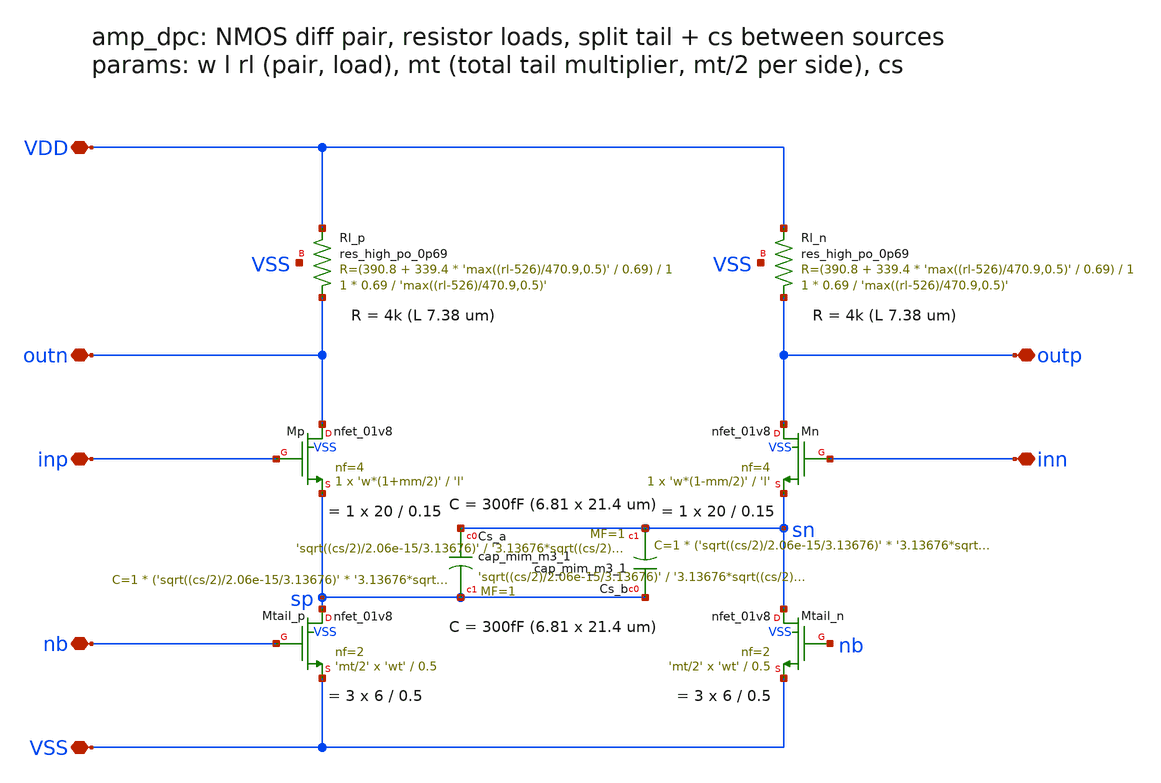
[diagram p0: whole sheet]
** sch_path: xschem/amp_dpc.sch
**.subckt amp_dpc VDD VSS nb inp inn outp outn
*.iopin VDD
*.iopin VSS
*.iopin nb
*.iopin inp
*.iopin inn
*.iopin outp
*.iopin outn
XRl_p outn VDD VSS sky130_fd_pr__res_high_po_0p69 L='max((rl-526)/470.9,0.5)' mult=1 m=1
XMp outn inp sp VSS sky130_fd_pr__nfet_01v8 L='l' W='w*(1+mm/2)' nf=4 ad='int((nf+1)/2) * W/nf * 0.29'
+ as='int((nf+2)/2) * W/nf * 0.29' pd='2*int((nf+1)/2) * (W/nf + 0.29)' ps='2*int((nf+2)/2) * (W/nf + 0.29)'
+ nrd='0.29 / W' nrs='0.29 / W' sa=0 sb=0 sd=0 mult=1 m=1
XMtail_p sp nb VSS VSS sky130_fd_pr__nfet_01v8 L=0.5 W='wt' nf=2 ad='int((nf+1)/2) * W/nf * 0.29' as='int((nf+2)/2) * W/nf * 0.29'
+ pd='2*int((nf+1)/2) * (W/nf + 0.29)' ps='2*int((nf+2)/2) * (W/nf + 0.29)' nrd='0.29 / W' nrs='0.29 / W'
+ sa=0 sb=0 sd=0 mult='mt/2' m='mt/2'
XRl_n outp VDD VSS sky130_fd_pr__res_high_po_0p69 L='max((rl-526)/470.9,0.5)' mult=1 m=1
XMn outp inn sn VSS sky130_fd_pr__nfet_01v8 L='l' W='w*(1-mm/2)' nf=4 ad='int((nf+1)/2) * W/nf * 0.29'
+ as='int((nf+2)/2) * W/nf * 0.29' pd='2*int((nf+1)/2) * (W/nf + 0.29)' ps='2*int((nf+2)/2) * (W/nf + 0.29)'
+ nrd='0.29 / W' nrs='0.29 / W' sa=0 sb=0 sd=0 mult=1 m=1
XMtail_n sn nb VSS VSS sky130_fd_pr__nfet_01v8 L=0.5 W='wt' nf=2 ad='int((nf+1)/2) * W/nf * 0.29' as='int((nf+2)/2) * W/nf * 0.29'
+ pd='2*int((nf+1)/2) * (W/nf + 0.29)' ps='2*int((nf+2)/2) * (W/nf + 0.29)' nrd='0.29 / W' nrs='0.29 / W'
+ sa=0 sb=0 sd=0 mult='mt/2' m='mt/2'
XCs_a sn sp sky130_fd_pr__cap_mim_m3_1 W='sqrt((cs/2)/2.06e-15/3.13676)' L='3.13676*sqrt((cs/2)/2.06e-15/3.13676)'
+ MF=1 m=1
XCs_b sp sn sky130_fd_pr__cap_mim_m3_1 W='sqrt((cs/2)/2.06e-15/3.13676)' L='3.13676*sqrt((cs/2)/2.06e-15/3.13676)'
+ MF=1 m=1
**.ends
.end
